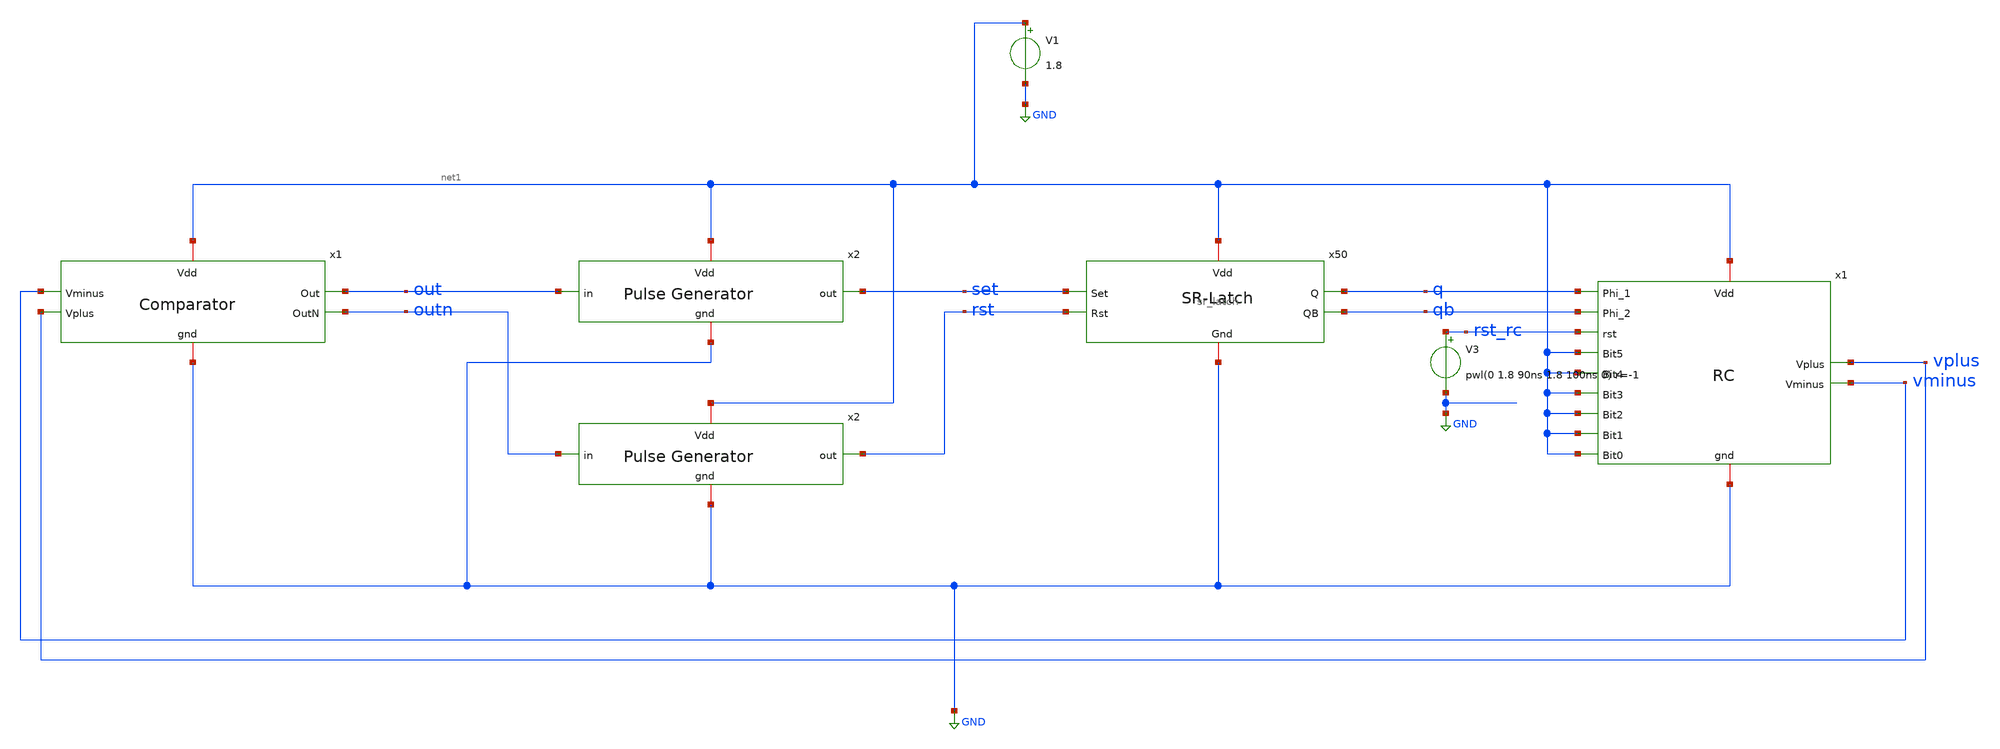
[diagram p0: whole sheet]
** sch_path: xschem/relax_oscillator_tb2.sch
**.subckt relax_oscillator_tb2
V1 net1 GND 1.8
V3 rst_rc GND pwl(0 1.8 90ns 1.8 100ns 0) r=-1
x5 net1 q qb rst_rc vplus vminus net1 net1 net1 net1 net1 net1 GND rc
x4 net1 set rst q qb GND sr_latch
x2 net1 set out GND pulse_generator
x3 net1 rst outn GND pulse_generator
x1 net1 out outn vminus vplus GND comparator
**** begin user architecture code



.lib /usr/local/share/pdk/sky130A/libs.tech/ngspice/sky130.lib.spice tt

.control
        tran 0.01n 10000ns
	plot v(rst_rc)
	plot v(out) v(outn)
	plot v(set) v(rst)
	plot v(vplus) v(vminus)
	linearize v(out)
	fft v(out)
	plot mag(v(out))
        meas tran iave INTEG i(v1) from=4ns to=5ns
        let power = -iave * 1.8 / 1ns
        print power
.endc
.save all


**** end user architecture code
**.ends
.GLOBAL GND
.end
